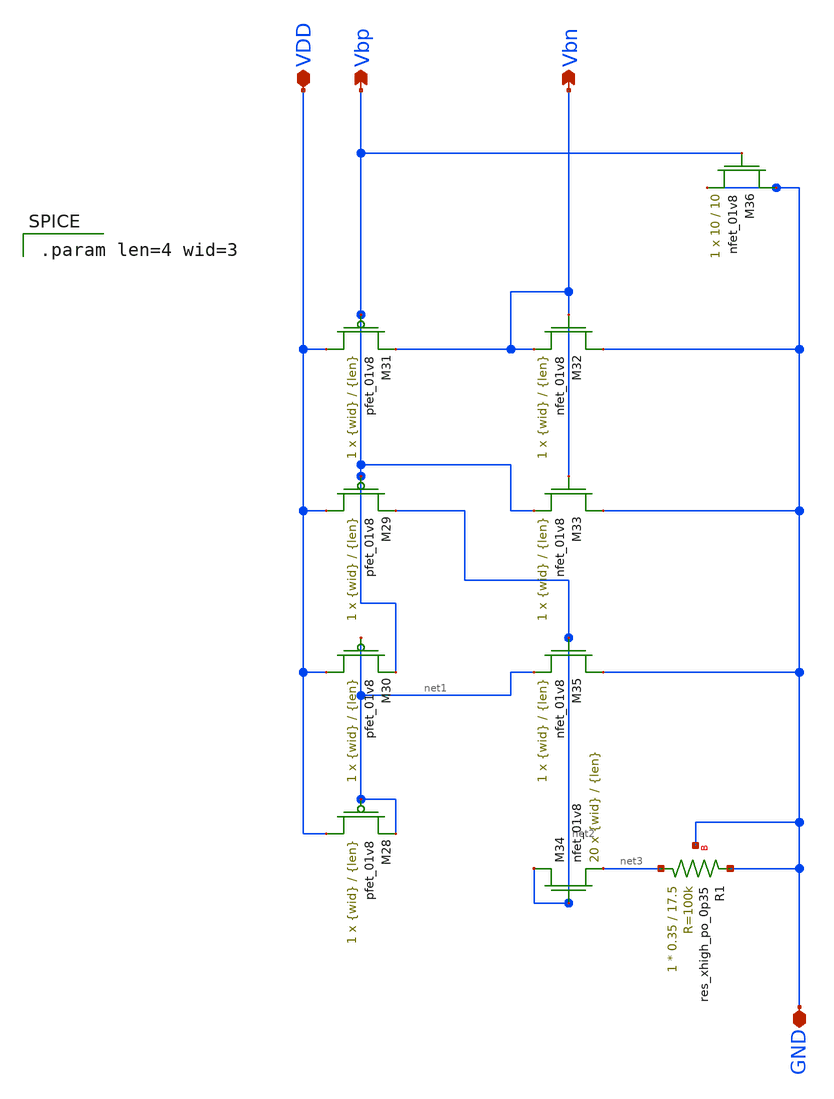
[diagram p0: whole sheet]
** sch_path: mp3/Layout_Schem_Designs/bias_gen_lds.sch
**.subckt bias_gen_lds Vbp VDD Vbn GND
*.opin Vbp
*.iopin VDD
*.opin Vbn
*.iopin GND
XM28 VDD net1 net1 VDD sky130_fd_pr__pfet_01v8 L={len} W={wid} nf=1 ad='int((nf+1)/2) * W/nf * 0.29'
+ as='int((nf+2)/2) * W/nf * 0.29' pd='2*int((nf+1)/2) * (W/nf + 0.29)' ps='2*int((nf+2)/2) * (W/nf + 0.29)'
+ nrd='0.29 / W' nrs='0.29 / W' sa=0 sb=0 sd=0 mult=1 m=1
XM29 VDD Vbp net2 VDD sky130_fd_pr__pfet_01v8 L={len} W={wid} nf=1 ad='int((nf+1)/2) * W/nf * 0.29' as='int((nf+2)/2) * W/nf * 0.29'
+ pd='2*int((nf+1)/2) * (W/nf + 0.29)' ps='2*int((nf+2)/2) * (W/nf + 0.29)' nrd='0.29 / W' nrs='0.29 / W'
+ sa=0 sb=0 sd=0 mult=1 m=1
XM30 VDD net1 Vbp VDD sky130_fd_pr__pfet_01v8 L={len} W={wid} nf=1 ad='int((nf+1)/2) * W/nf * 0.29' as='int((nf+2)/2) * W/nf * 0.29'
+ pd='2*int((nf+1)/2) * (W/nf + 0.29)' ps='2*int((nf+2)/2) * (W/nf + 0.29)' nrd='0.29 / W' nrs='0.29 / W'
+ sa=0 sb=0 sd=0 mult=1 m=1
XM31 VDD Vbp Vbn VDD sky130_fd_pr__pfet_01v8 L={len} W={wid} nf=1 ad='int((nf+1)/2) * W/nf * 0.29' as='int((nf+2)/2) * W/nf * 0.29'
+ pd='2*int((nf+1)/2) * (W/nf + 0.29)' ps='2*int((nf+2)/2) * (W/nf + 0.29)' nrd='0.29 / W' nrs='0.29 / W'
+ sa=0 sb=0 sd=0 mult=1 m=1
XM32 GND Vbn Vbn GND sky130_fd_pr__nfet_01v8 L={len} W={wid} nf=1 ad='int((nf+1)/2) * W/nf * 0.29' as='int((nf+2)/2) * W/nf * 0.29'
+ pd='2*int((nf+1)/2) * (W/nf + 0.29)' ps='2*int((nf+2)/2) * (W/nf + 0.29)' nrd='0.29 / W' nrs='0.29 / W'
+ sa=0 sb=0 sd=0 mult=1 m=1
XM33 GND Vbn Vbp GND sky130_fd_pr__nfet_01v8 L={len} W={wid} nf=1 ad='int((nf+1)/2) * W/nf * 0.29' as='int((nf+2)/2) * W/nf * 0.29'
+ pd='2*int((nf+1)/2) * (W/nf + 0.29)' ps='2*int((nf+2)/2) * (W/nf + 0.29)' nrd='0.29 / W' nrs='0.29 / W'
+ sa=0 sb=0 sd=0 mult=1 m=1
XM34 net2 net2 net3 GND sky130_fd_pr__nfet_01v8 L={len} W={wid} nf=1 ad='int((nf+1)/2) * W/nf * 0.29'
+ as='int((nf+2)/2) * W/nf * 0.29' pd='2*int((nf+1)/2) * (W/nf + 0.29)' ps='2*int((nf+2)/2) * (W/nf + 0.29)'
+ nrd='0.29 / W' nrs='0.29 / W' sa=0 sb=0 sd=0 mult=20 m=20
XM35 GND net2 net1 GND sky130_fd_pr__nfet_01v8 L={len} W={wid} nf=1 ad='int((nf+1)/2) * W/nf * 0.29'
+ as='int((nf+2)/2) * W/nf * 0.29' pd='2*int((nf+1)/2) * (W/nf + 0.29)' ps='2*int((nf+2)/2) * (W/nf + 0.29)'
+ nrd='0.29 / W' nrs='0.29 / W' sa=0 sb=0 sd=0 mult=1 m=1
XM36 GND Vbp GND GND sky130_fd_pr__nfet_01v8 L=10 W=10 nf=1 ad='int((nf+1)/2) * W/nf * 0.29' as='int((nf+2)/2) * W/nf * 0.29'
+ pd='2*int((nf+1)/2) * (W/nf + 0.29)' ps='2*int((nf+2)/2) * (W/nf + 0.29)' nrd='0.29 / W' nrs='0.29 / W'
+ sa=0 sb=0 sd=0 mult=1 m=1
XR1 net3 GND GND sky130_fd_pr__res_xhigh_po_0p35 L=17.5 mult=1 m=1
**** begin user architecture code

.param len=4 wid=3

**** end user architecture code
**.ends
.end
